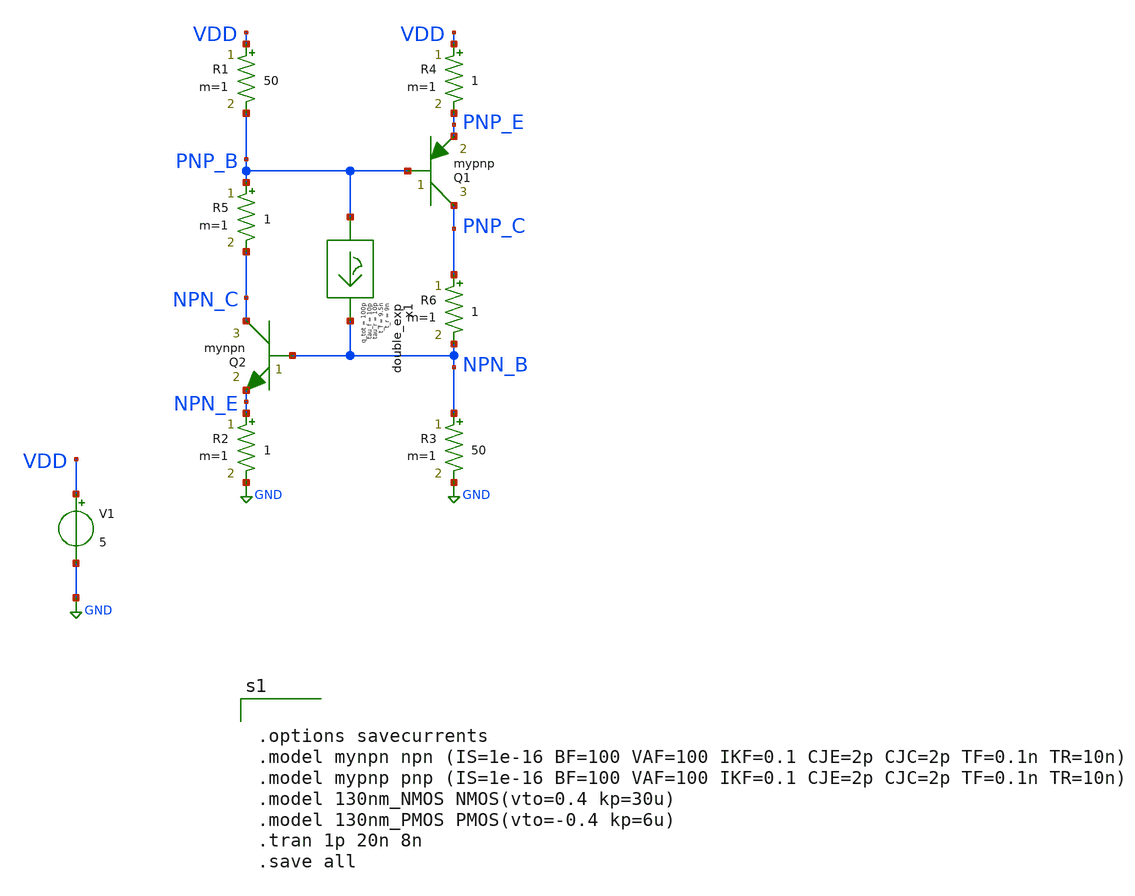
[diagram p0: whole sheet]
** sch_path: latchup/intermediate.sch
**.subckt intermediate
Q1 PNP_C PNP_B PNP_E mypnp area=1 m=1
Q2 NPN_C NPN_B NPN_E mynpn area=1 m=1
R3 NPN_B GND 50 m=1
R4 VDD PNP_E 1 m=1
V1 VDD GND 5
x1 PNP_B NPN_B double_exp t_r=9n tau_r=10p t_f=9.5n tau_f=10p q_tot=100p
R1 VDD PNP_B 50 m=1
R2 NPN_E GND 1 m=1
R5 PNP_B NPN_C 1 m=1
R6 PNP_C NPN_B 1 m=1
**** begin user architecture code


.options savecurrents
.model mynpn npn (IS=1e-16 BF=100 VAF=100 IKF=0.1 CJE=2p CJC=2p TF=0.1n TR=10n)
.model mypnp pnp (IS=1e-16 BF=100 VAF=100 IKF=0.1 CJE=2p CJC=2p TF=0.1n TR=10n)
.model 130nm_NMOS NMOS(vto=0.4 kp=30u)
.model 130nm_PMOS PMOS(vto=-0.4 kp=6u)
.tran 1p 20n 8n
.save all




.include /usr/local/share/rad_modeling_blocks/rad_modeling_blocks.spice


**** end user architecture code
**.ends

* expanding   symbol:  double_exp.sym # of pins=2
** sym_path: xschem_rad_library/double_exp.sym
** sch_path: xschem_rad_library/double_exp.sch
.subckt double_exp in out  t_r=0 t_f=0 tau_r=0 tau_f=0 q_tot=0
*.opin OUT
*.ipin IN
I1 IN OUT EXP(0 {q_tot / (t_f-t_r+tau_f-tau_r)} {t_r} {tau_r} {t_f} {tau_f})
.ends

.GLOBAL GND
.end
